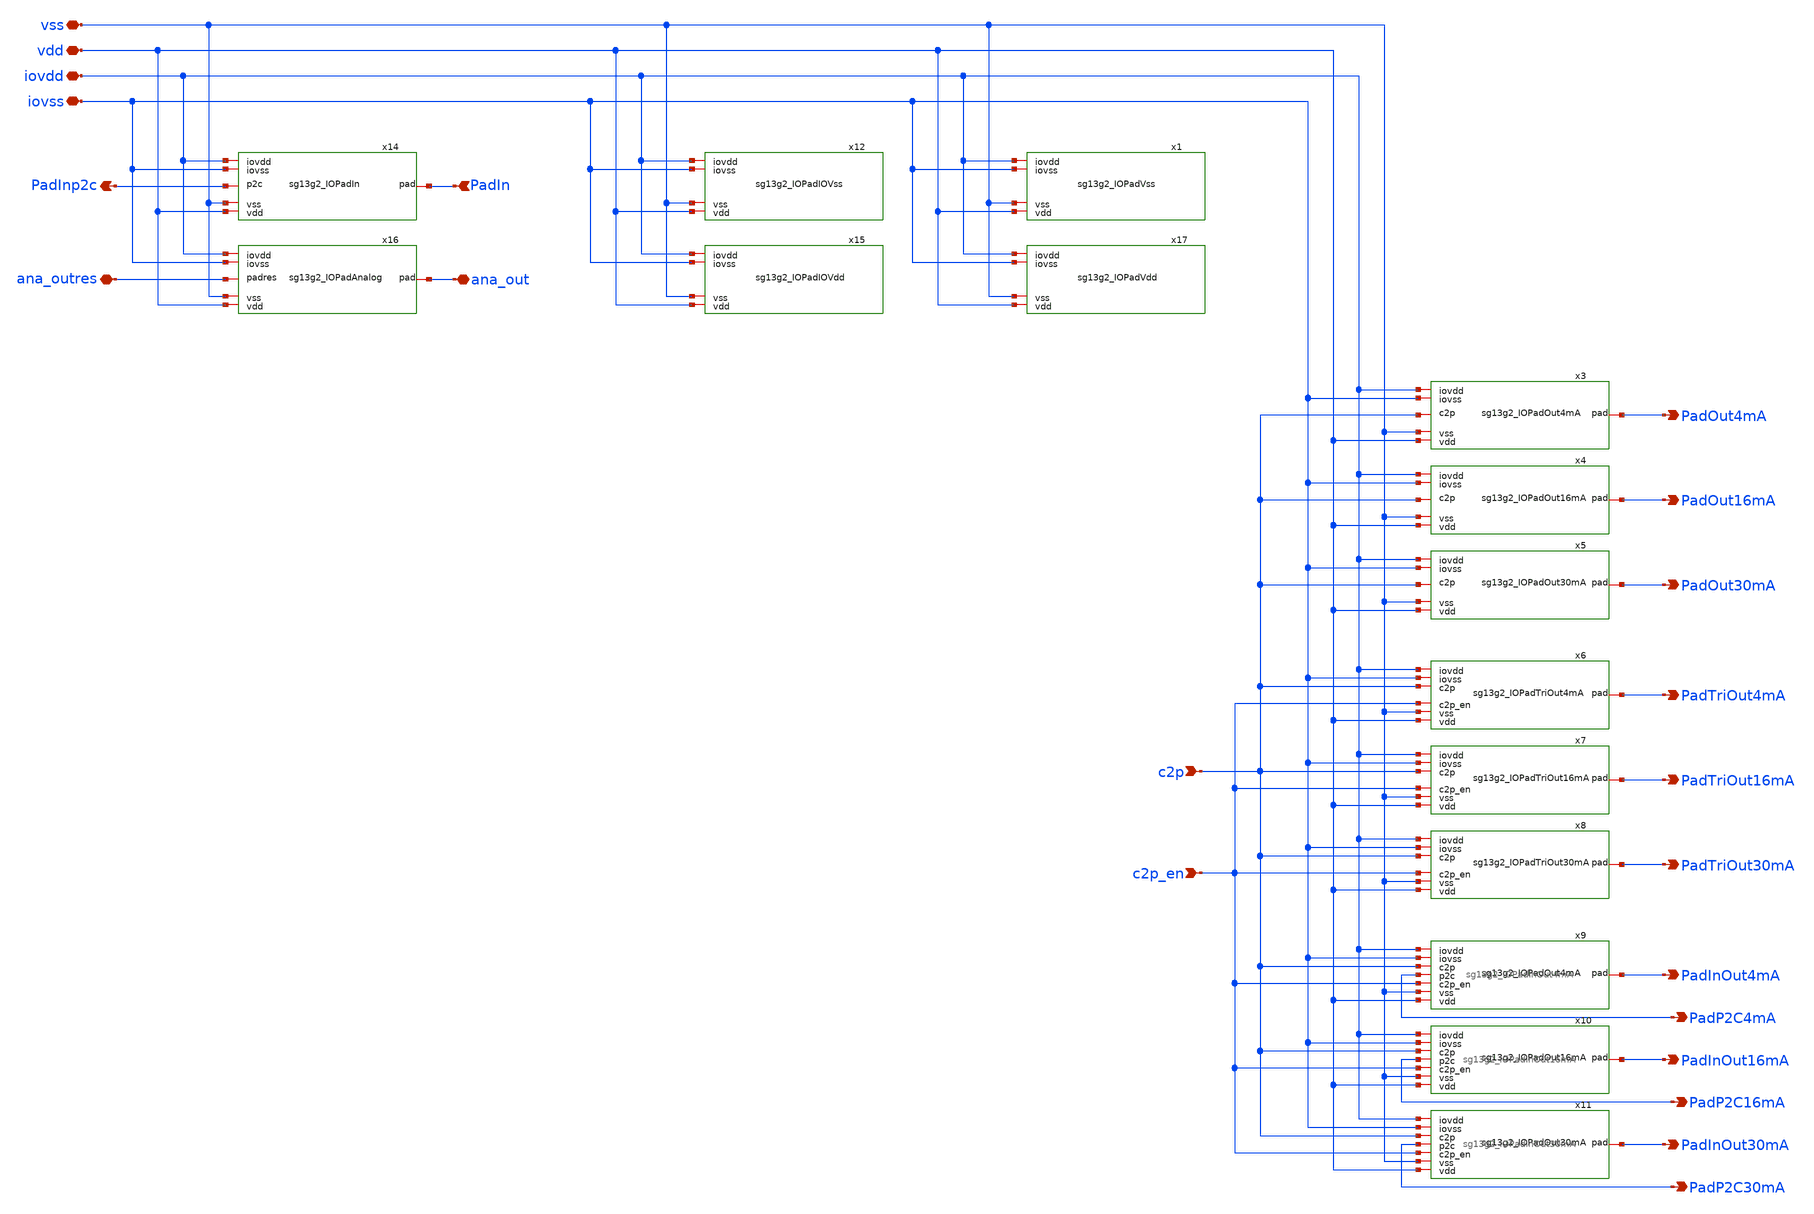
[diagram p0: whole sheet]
** sch_path: ihp-sg13g2/libs.ref/sg13g2_io/xschem/sg13g2_Gallery.sch
**.subckt sg13g2_Gallery ana_out ana_outres vdd iovdd vss iovss c2p PadOut4mA c2p_en PadOut16mA
*+ PadOut30mA PadTriOut4mA PadTriOut16mA PadTriOut30mA PadInOut4mA PadInOut16mA PadInOut30mA PadP2C4mA PadP2C16mA
*+ PadP2C30mA PadIn PadInp2c
*.iopin ana_out
*.iopin ana_outres
*.iopin vdd
*.iopin iovdd
*.iopin vss
*.iopin iovss
*.ipin c2p
*.opin PadOut4mA
*.ipin c2p_en
*.opin PadOut16mA
*.opin PadOut30mA
*.opin PadTriOut4mA
*.opin PadTriOut16mA
*.opin PadTriOut30mA
*.opin PadInOut4mA
*.opin PadInOut16mA
*.opin PadInOut30mA
*.opin PadP2C4mA
*.opin PadP2C16mA
*.opin PadP2C30mA
*.ipin PadIn
*.opin PadInp2c
x1 iovdd iovss vss vdd sg13g2_IOPadVSS
x3 iovdd iovss c2p vss vdd PadOut4mA sg13g2_IOPadOut4mA
x4 iovdd iovss c2p vss vdd PadOut16mA sg13g2_IOPadOut16mA
x5 iovdd iovss c2p vss vdd PadOut30mA sg13g2_IOPadOut30mA
x6 iovdd iovss c2p c2p_en vss vdd PadTriOut4mA sg13g2_IOPadTriOut4mA
x7 iovdd iovss c2p c2p_en vss vdd PadTriOut16mA sg13g2_IOPadTriOut16mA
x8 iovdd iovss c2p c2p_en vss vdd PadTriOut30mA sg13g2_IOPadTriOut30mA
x9 iovdd iovss c2p PadP2C4mA c2p_en vss vdd PadInOut4mA sg13g2_IOPadInOut4mA
x10 iovdd iovss c2p PadP2C16mA c2p_en vss vdd PadInOut16mA sg13g2_IOPadInOut16mA
x11 iovdd iovss c2p PadP2C30mA c2p_en vss vdd PadInOut30mA sg13g2_IOPadInOut30mA
x12 iovdd iovss vss vdd sg13g2_IOPadIOVss
x16 iovdd iovss ana_outres vss vdd ana_out sg13g2_IOPadAnalog
x14 iovdd iovss PadInp2c vss vdd PadIn sg13g2_IOPadIn
x15 iovdd iovss vss vdd sg13g2_IOPadIOVdd
x17 iovdd iovss vss vdd sg13g2_IOPadVdd
**.ends
.end
